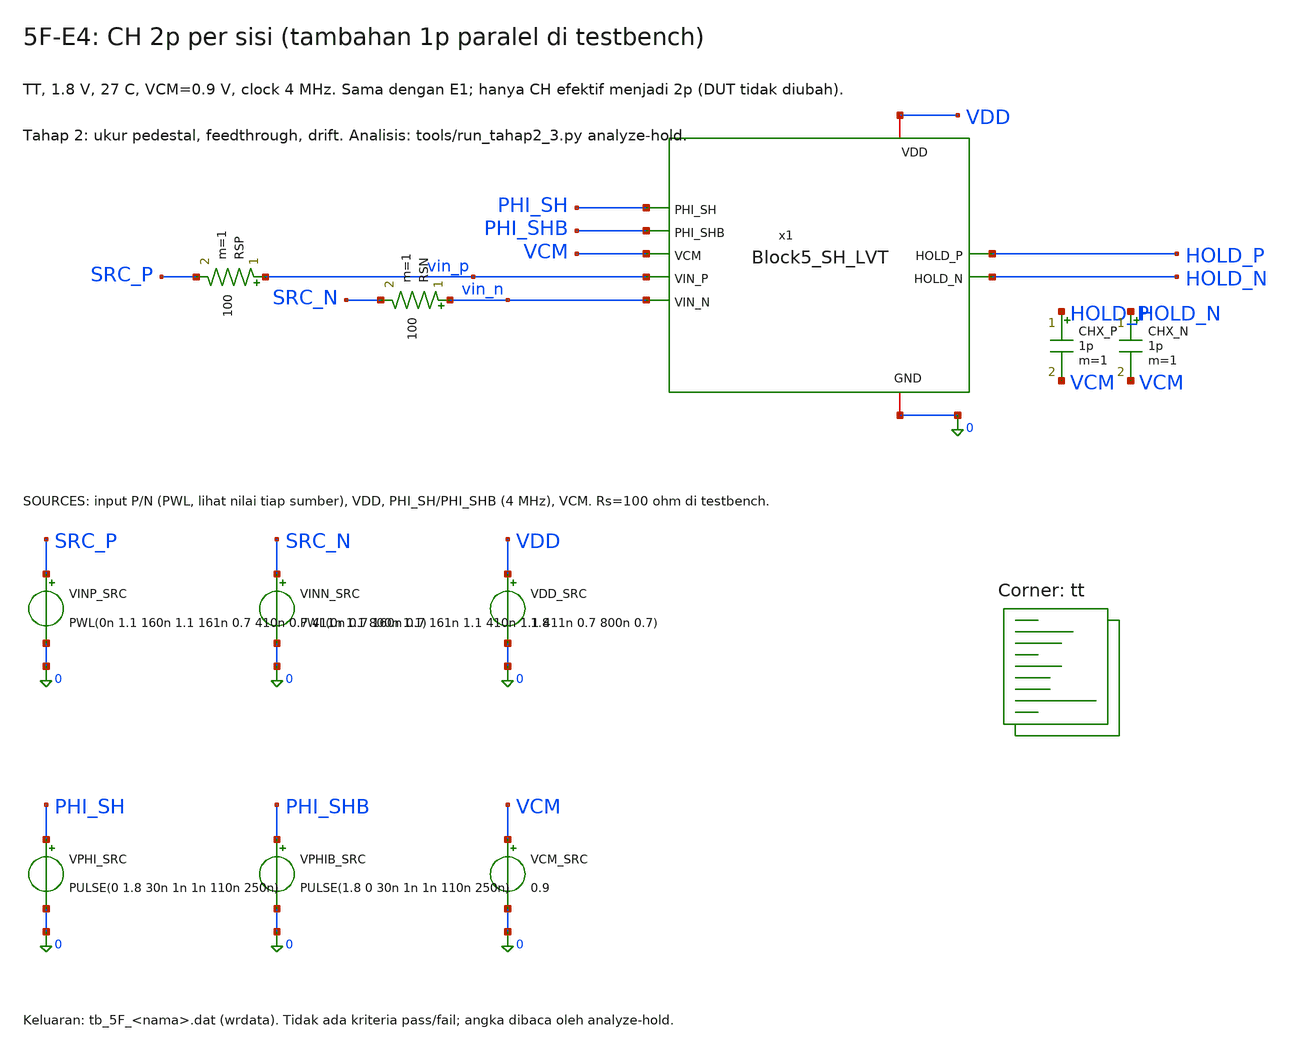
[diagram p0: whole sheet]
** sch_path: blocks/05_Switch_Network/sim/tb_5F_E4_ch_2p.sch
**.subckt tb_5F_E4_ch_2p
RSP vin_p SRC_P 100 m=1
RSN vin_n SRC_N 100 m=1
VINP_SRC SRC_P 0 PWL(0n 1.1 160n 1.1 161n 0.7 410n 0.7 411n 1.1 800n 1.1)
VINN_SRC SRC_N 0 PWL(0n 0.7 160n 0.7 161n 1.1 410n 1.1 411n 0.7 800n 0.7)
VDD_SRC VDD 0 1.8
VPHI_SRC PHI_SH 0 PULSE(0 1.8 30n 1n 1n 110n 250n)
VPHIB_SRC PHI_SHB 0 PULSE(1.8 0 30n 1n 1n 110n 250n)
VCM_SRC VCM 0 0.9
x1 VDD PHI_SH PHI_SHB 0 VCM vin_p HOLD_P HOLD_N vin_n Block5_SH_LVT
CHX_P HOLD_P VCM 1p m=1
CHX_N HOLD_N VCM 1p m=1
**** begin user architecture code
.lib $::SKYWATER_MODELS/sky130.lib.spice tt


* E4_ch_2p: diagnosa hold error Block 5 (tahap 2). TT, 1.8 V, 27 C.
* .ic hanya kondisi awal numerik, bukan rangkaian reset.
.option scale=1e-6 reltol=1e-5 abstol=1e-15 vntol=1e-8
.temp 27
.ic V(HOLD_P)=0.9 V(HOLD_N)=0.9
.control
save all
set wr_singlescale
set wr_vecnames
set numdgt=15
tran 0.1n 700n 0 0.1n
wrdata tb_5F_E4_ch_2p.dat v(SRC_P) v(SRC_N) v(VIN_P) v(VIN_N) v(HOLD_P) v(HOLD_N) v(PHI_SH)
+ v(PHI_SHB)
echo TB_5F_DONE
.endc


**** end user architecture code
**.ends

* expanding   symbol:  blocks/05_Switch_Network/xschem/Block5_SH_LVT.sym # of pins=9
** sym_path: blocks/05_Switch_Network/xschem/Block5_SH_LVT.sym
** sch_path: blocks/05_Switch_Network/xschem/Block5_SH_LVT.sch
.subckt Block5_SH_LVT VDD PHI_SH PHI_SHB GND VCM VIN_P HOLD_P HOLD_N VIN_N
*.ipin VIN_P
*.ipin VIN_N
*.ipin PHI_SH
*.ipin PHI_SHB
*.iopin VDD
*.iopin GND
*.ipin VCM
*.opin HOLD_P
*.opin HOLD_N
CH_P HOLD_P VCM 1p m=1
CH_N HOLD_N VCM 1p m=1
x3 VIN_P HOLD_P PHI_SHB PHI_SH VDD GND TG_SC_LVT
x1 VIN_N HOLD_N PHI_SHB PHI_SH VDD GND TG_SC_LVT
.ends


* expanding   symbol:  blocks/05_Switch_Network/xschem/TG_SC_LVT.sym # of pins=6
** sym_path: blocks/05_Switch_Network/xschem/TG_SC_LVT.sym
** sch_path: blocks/05_Switch_Network/xschem/TG_SC_LVT.sch
.subckt TG_SC_LVT A B CLK_P CLK_N VDD GND
*.iopin A
*.iopin B
*.ipin CLK_P
*.ipin CLK_N
*.iopin VDD
*.iopin GND
XMP A CLK_P B VDD sky130_fd_pr__pfet_01v8_lvt L=0.35 W=8 nf=1 ad='int((1 + 1)/2) * 8 / 1 * 0.29' as='int((1 + 2)/2) * 8 / 1 * 0.29'
+ pd='2*int((1 + 1)/2) * (8 / 1 + 0.29)' ps='2*int((1 + 2)/2) * (8 / 1 + 0.29)' nrd='0.29 / 8 ' nrs='0.29 / 8 '
+ sa=0 sb=0 sd=0 mult=1
XMN A CLK_N B GND sky130_fd_pr__nfet_01v8_lvt L=0.15 W=4 nf=1 ad='int((1 + 1)/2) * 4 / 1 * 0.29' as='int((1 + 2)/2) * 4 / 1 * 0.29'
+ pd='2*int((1 + 1)/2) * (4 / 1 + 0.29)' ps='2*int((1 + 2)/2) * (4 / 1 + 0.29)' nrd='0.29 / 4 ' nrs='0.29 / 4 '
+ sa=0 sb=0 sd=0 mult=1
.ends

.end
